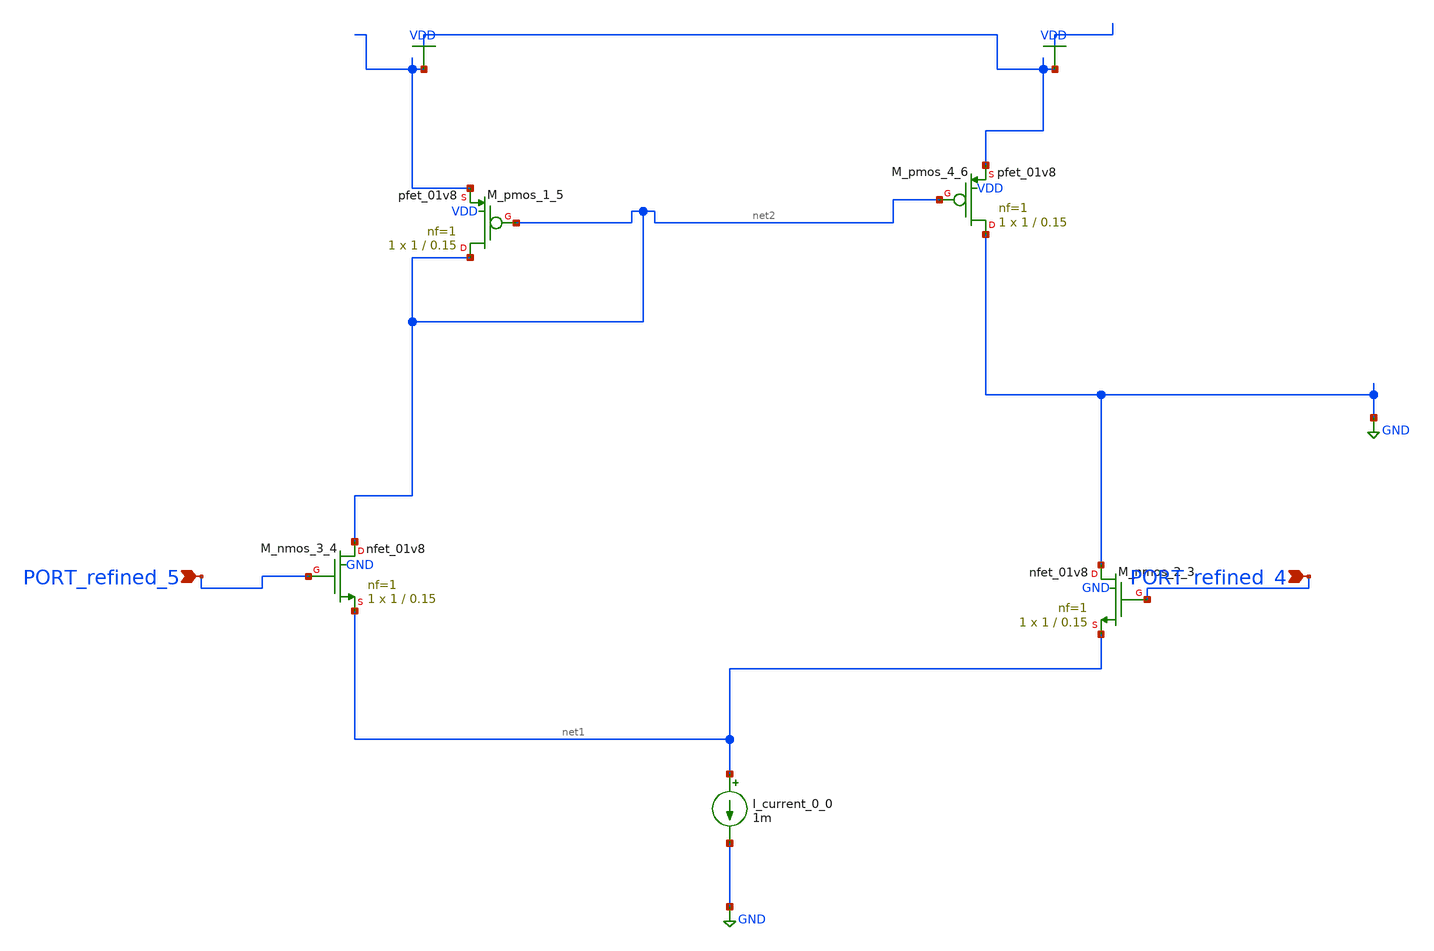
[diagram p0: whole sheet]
** sch_path: schematics/AMSNet/281.sch
**.subckt 281 PORT_refined_4 PORT_refined_5
*.ipin PORT_refined_4
*.ipin PORT_refined_5
I_current_0_0 net1 GND 1m
XM_nmos_2_3 GND PORT_refined_4 net1 GND sky130_fd_pr__nfet_01v8 L=0.15 W=1 nf=1 ad='int((1 + 1)/2) * 1 / 1 * 0.29'
+ as='int((1 + 2)/2) * 1 / 1 * 0.29' pd='2*int((1 + 1)/2) * (1 / 1 + 0.29)' ps='2*int((1 + 2)/2) * (1 / 1 + 0.29)'
+ nrd='0.29 / 1 ' nrs='0.29 / 1 ' sa=0 sb=0 sd=0 mult=1 m=1
XM_nmos_3_4 net2 PORT_refined_5 net1 GND sky130_fd_pr__nfet_01v8 L=0.15 W=1 nf=1 ad='int((1 + 1)/2) * 1 / 1 * 0.29'
+ as='int((1 + 2)/2) * 1 / 1 * 0.29' pd='2*int((1 + 1)/2) * (1 / 1 + 0.29)' ps='2*int((1 + 2)/2) * (1 / 1 + 0.29)'
+ nrd='0.29 / 1 ' nrs='0.29 / 1 ' sa=0 sb=0 sd=0 mult=1 m=1
XM_pmos_1_5 net2 net2 VDD VDD sky130_fd_pr__pfet_01v8 L=0.15 W=1 nf=1 ad='int((1 + 1)/2) * 1 / 1 * 0.29'
+ as='int((1 + 2)/2) * 1 / 1 * 0.29' pd='2*int((1 + 1)/2) * (1 / 1 + 0.29)' ps='2*int((1 + 2)/2) * (1 / 1 + 0.29)'
+ nrd='0.29 / 1 ' nrs='0.29 / 1 ' sa=0 sb=0 sd=0 mult=1 m=1
XM_pmos_4_6 GND net2 VDD VDD sky130_fd_pr__pfet_01v8 L=0.15 W=1 nf=1 ad='int((1 + 1)/2) * 1 / 1 * 0.29'
+ as='int((1 + 2)/2) * 1 / 1 * 0.29' pd='2*int((1 + 1)/2) * (1 / 1 + 0.29)' ps='2*int((1 + 2)/2) * (1 / 1 + 0.29)'
+ nrd='0.29 / 1 ' nrs='0.29 / 1 ' sa=0 sb=0 sd=0 mult=1 m=1
**.ends
.GLOBAL GND
.GLOBAL VDD
.end
